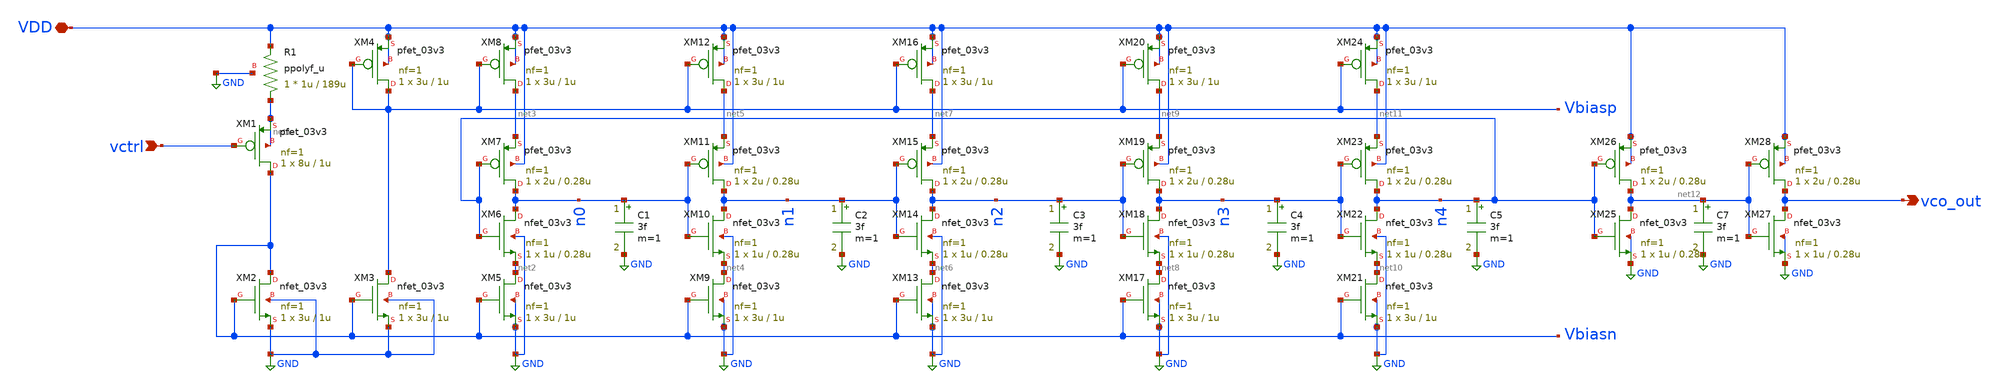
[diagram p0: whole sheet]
** sch_path: analog/vco/vco_core.sch
**.subckt vco_core VDD vctrl vco_out
*.iopin VDD
*.ipin vctrl
*.opin vco_out
XM1 Vbiasn vctrl net1 net1 pfet_03v3 L=1u W=8u nf=1 ad='int((nf+1)/2) * W/nf * 0.18u' as='int((nf+2)/2) * W/nf * 0.18u'
+ pd='2*int((nf+1)/2) * (W/nf + 0.18u)' ps='2*int((nf+2)/2) * (W/nf + 0.18u)' nrd='0.18u / W' nrs='0.18u / W'
+ sa=0 sb=0 sd=0 m=1
XM2 Vbiasn Vbiasn GND GND nfet_03v3 L=1u W=3u nf=1 ad='int((nf+1)/2) * W/nf * 0.18u' as='int((nf+2)/2) * W/nf * 0.18u'
+ pd='2*int((nf+1)/2) * (W/nf + 0.18u)' ps='2*int((nf+2)/2) * (W/nf + 0.18u)' nrd='0.18u / W' nrs='0.18u / W'
+ sa=0 sb=0 sd=0 m=1
XM3 Vbiasp Vbiasn GND GND nfet_03v3 L=1u W=3u nf=1 ad='int((nf+1)/2) * W/nf * 0.18u' as='int((nf+2)/2) * W/nf * 0.18u'
+ pd='2*int((nf+1)/2) * (W/nf + 0.18u)' ps='2*int((nf+2)/2) * (W/nf + 0.18u)' nrd='0.18u / W' nrs='0.18u / W'
+ sa=0 sb=0 sd=0 m=1
XM4 Vbiasp Vbiasp VDD VDD pfet_03v3 L=1u W=3u nf=1 ad='int((nf+1)/2) * W/nf * 0.18u' as='int((nf+2)/2) * W/nf * 0.18u'
+ pd='2*int((nf+1)/2) * (W/nf + 0.18u)' ps='2*int((nf+2)/2) * (W/nf + 0.18u)' nrd='0.18u / W' nrs='0.18u / W'
+ sa=0 sb=0 sd=0 m=1
XR1 net1 VDD GND ppolyf_u r_width=1u r_length=189u m=1
XM5 net2 Vbiasn GND GND nfet_03v3 L=1u W=3u nf=1 ad='int((nf+1)/2) * W/nf * 0.18u' as='int((nf+2)/2) * W/nf * 0.18u'
+ pd='2*int((nf+1)/2) * (W/nf + 0.18u)' ps='2*int((nf+2)/2) * (W/nf + 0.18u)' nrd='0.18u / W' nrs='0.18u / W'
+ sa=0 sb=0 sd=0 m=1
XM6 n0 n4 net2 GND nfet_03v3 L=0.28u W=1u nf=1 ad='int((nf+1)/2) * W/nf * 0.18u' as='int((nf+2)/2) * W/nf * 0.18u'
+ pd='2*int((nf+1)/2) * (W/nf + 0.18u)' ps='2*int((nf+2)/2) * (W/nf + 0.18u)' nrd='0.18u / W' nrs='0.18u / W'
+ sa=0 sb=0 sd=0 m=1
XM7 n0 n4 net3 VDD pfet_03v3 L=0.28u W=2u nf=1 ad='int((nf+1)/2) * W/nf * 0.18u' as='int((nf+2)/2) * W/nf * 0.18u'
+ pd='2*int((nf+1)/2) * (W/nf + 0.18u)' ps='2*int((nf+2)/2) * (W/nf + 0.18u)' nrd='0.18u / W' nrs='0.18u / W'
+ sa=0 sb=0 sd=0 m=1
XM8 net3 Vbiasp VDD VDD pfet_03v3 L=1u W=3u nf=1 ad='int((nf+1)/2) * W/nf * 0.18u' as='int((nf+2)/2) * W/nf * 0.18u'
+ pd='2*int((nf+1)/2) * (W/nf + 0.18u)' ps='2*int((nf+2)/2) * (W/nf + 0.18u)' nrd='0.18u / W' nrs='0.18u / W'
+ sa=0 sb=0 sd=0 m=1
XM9 net4 Vbiasn GND GND nfet_03v3 L=1u W=3u nf=1 ad='int((nf+1)/2) * W/nf * 0.18u' as='int((nf+2)/2) * W/nf * 0.18u'
+ pd='2*int((nf+1)/2) * (W/nf + 0.18u)' ps='2*int((nf+2)/2) * (W/nf + 0.18u)' nrd='0.18u / W' nrs='0.18u / W'
+ sa=0 sb=0 sd=0 m=1
XM10 n1 n0 net4 GND nfet_03v3 L=0.28u W=1u nf=1 ad='int((nf+1)/2) * W/nf * 0.18u' as='int((nf+2)/2) * W/nf * 0.18u'
+ pd='2*int((nf+1)/2) * (W/nf + 0.18u)' ps='2*int((nf+2)/2) * (W/nf + 0.18u)' nrd='0.18u / W' nrs='0.18u / W'
+ sa=0 sb=0 sd=0 m=1
XM11 n1 n0 net5 VDD pfet_03v3 L=0.28u W=2u nf=1 ad='int((nf+1)/2) * W/nf * 0.18u' as='int((nf+2)/2) * W/nf * 0.18u'
+ pd='2*int((nf+1)/2) * (W/nf + 0.18u)' ps='2*int((nf+2)/2) * (W/nf + 0.18u)' nrd='0.18u / W' nrs='0.18u / W'
+ sa=0 sb=0 sd=0 m=1
XM12 net5 Vbiasp VDD VDD pfet_03v3 L=1u W=3u nf=1 ad='int((nf+1)/2) * W/nf * 0.18u' as='int((nf+2)/2) * W/nf * 0.18u'
+ pd='2*int((nf+1)/2) * (W/nf + 0.18u)' ps='2*int((nf+2)/2) * (W/nf + 0.18u)' nrd='0.18u / W' nrs='0.18u / W'
+ sa=0 sb=0 sd=0 m=1
XM13 net6 Vbiasn GND GND nfet_03v3 L=1u W=3u nf=1 ad='int((nf+1)/2) * W/nf * 0.18u' as='int((nf+2)/2) * W/nf * 0.18u'
+ pd='2*int((nf+1)/2) * (W/nf + 0.18u)' ps='2*int((nf+2)/2) * (W/nf + 0.18u)' nrd='0.18u / W' nrs='0.18u / W'
+ sa=0 sb=0 sd=0 m=1
XM14 n2 n1 net6 GND nfet_03v3 L=0.28u W=1u nf=1 ad='int((nf+1)/2) * W/nf * 0.18u' as='int((nf+2)/2) * W/nf * 0.18u'
+ pd='2*int((nf+1)/2) * (W/nf + 0.18u)' ps='2*int((nf+2)/2) * (W/nf + 0.18u)' nrd='0.18u / W' nrs='0.18u / W'
+ sa=0 sb=0 sd=0 m=1
XM15 n2 n1 net7 VDD pfet_03v3 L=0.28u W=2u nf=1 ad='int((nf+1)/2) * W/nf * 0.18u' as='int((nf+2)/2) * W/nf * 0.18u'
+ pd='2*int((nf+1)/2) * (W/nf + 0.18u)' ps='2*int((nf+2)/2) * (W/nf + 0.18u)' nrd='0.18u / W' nrs='0.18u / W'
+ sa=0 sb=0 sd=0 m=1
XM16 net7 Vbiasp VDD VDD pfet_03v3 L=1u W=3u nf=1 ad='int((nf+1)/2) * W/nf * 0.18u' as='int((nf+2)/2) * W/nf * 0.18u'
+ pd='2*int((nf+1)/2) * (W/nf + 0.18u)' ps='2*int((nf+2)/2) * (W/nf + 0.18u)' nrd='0.18u / W' nrs='0.18u / W'
+ sa=0 sb=0 sd=0 m=1
XM17 net8 Vbiasn GND GND nfet_03v3 L=1u W=3u nf=1 ad='int((nf+1)/2) * W/nf * 0.18u' as='int((nf+2)/2) * W/nf * 0.18u'
+ pd='2*int((nf+1)/2) * (W/nf + 0.18u)' ps='2*int((nf+2)/2) * (W/nf + 0.18u)' nrd='0.18u / W' nrs='0.18u / W'
+ sa=0 sb=0 sd=0 m=1
XM18 n3 n2 net8 GND nfet_03v3 L=0.28u W=1u nf=1 ad='int((nf+1)/2) * W/nf * 0.18u' as='int((nf+2)/2) * W/nf * 0.18u'
+ pd='2*int((nf+1)/2) * (W/nf + 0.18u)' ps='2*int((nf+2)/2) * (W/nf + 0.18u)' nrd='0.18u / W' nrs='0.18u / W'
+ sa=0 sb=0 sd=0 m=1
XM19 n3 n2 net9 VDD pfet_03v3 L=0.28u W=2u nf=1 ad='int((nf+1)/2) * W/nf * 0.18u' as='int((nf+2)/2) * W/nf * 0.18u'
+ pd='2*int((nf+1)/2) * (W/nf + 0.18u)' ps='2*int((nf+2)/2) * (W/nf + 0.18u)' nrd='0.18u / W' nrs='0.18u / W'
+ sa=0 sb=0 sd=0 m=1
XM20 net9 Vbiasp VDD VDD pfet_03v3 L=1u W=3u nf=1 ad='int((nf+1)/2) * W/nf * 0.18u' as='int((nf+2)/2) * W/nf * 0.18u'
+ pd='2*int((nf+1)/2) * (W/nf + 0.18u)' ps='2*int((nf+2)/2) * (W/nf + 0.18u)' nrd='0.18u / W' nrs='0.18u / W'
+ sa=0 sb=0 sd=0 m=1
XM21 net10 Vbiasn GND GND nfet_03v3 L=1u W=3u nf=1 ad='int((nf+1)/2) * W/nf * 0.18u' as='int((nf+2)/2) * W/nf * 0.18u'
+ pd='2*int((nf+1)/2) * (W/nf + 0.18u)' ps='2*int((nf+2)/2) * (W/nf + 0.18u)' nrd='0.18u / W' nrs='0.18u / W'
+ sa=0 sb=0 sd=0 m=1
XM22 n4 n3 net10 GND nfet_03v3 L=0.28u W=1u nf=1 ad='int((nf+1)/2) * W/nf * 0.18u' as='int((nf+2)/2) * W/nf * 0.18u'
+ pd='2*int((nf+1)/2) * (W/nf + 0.18u)' ps='2*int((nf+2)/2) * (W/nf + 0.18u)' nrd='0.18u / W' nrs='0.18u / W'
+ sa=0 sb=0 sd=0 m=1
XM23 n4 n3 net11 VDD pfet_03v3 L=0.28u W=2u nf=1 ad='int((nf+1)/2) * W/nf * 0.18u' as='int((nf+2)/2) * W/nf * 0.18u'
+ pd='2*int((nf+1)/2) * (W/nf + 0.18u)' ps='2*int((nf+2)/2) * (W/nf + 0.18u)' nrd='0.18u / W' nrs='0.18u / W'
+ sa=0 sb=0 sd=0 m=1
XM24 net11 Vbiasp VDD VDD pfet_03v3 L=1u W=3u nf=1 ad='int((nf+1)/2) * W/nf * 0.18u' as='int((nf+2)/2) * W/nf * 0.18u'
+ pd='2*int((nf+1)/2) * (W/nf + 0.18u)' ps='2*int((nf+2)/2) * (W/nf + 0.18u)' nrd='0.18u / W' nrs='0.18u / W'
+ sa=0 sb=0 sd=0 m=1
C1 n0 GND 3f m=1
C2 n1 GND 3f m=1
C3 n2 GND 3f m=1
C4 n3 GND 3f m=1
C5 n4 GND 3f m=1
XM25 net12 n4 GND GND nfet_03v3 L=0.28u W=1u nf=1 ad='int((nf+1)/2) * W/nf * 0.18u' as='int((nf+2)/2) * W/nf * 0.18u'
+ pd='2*int((nf+1)/2) * (W/nf + 0.18u)' ps='2*int((nf+2)/2) * (W/nf + 0.18u)' nrd='0.18u / W' nrs='0.18u / W'
+ sa=0 sb=0 sd=0 m=1
XM26 net12 n4 VDD VDD pfet_03v3 L=0.28u W=2u nf=1 ad='int((nf+1)/2) * W/nf * 0.18u' as='int((nf+2)/2) * W/nf * 0.18u'
+ pd='2*int((nf+1)/2) * (W/nf + 0.18u)' ps='2*int((nf+2)/2) * (W/nf + 0.18u)' nrd='0.18u / W' nrs='0.18u / W'
+ sa=0 sb=0 sd=0 m=1
XM27 vco_out net12 GND GND nfet_03v3 L=0.28u W=1u nf=1 ad='int((nf+1)/2) * W/nf * 0.18u' as='int((nf+2)/2) * W/nf * 0.18u'
+ pd='2*int((nf+1)/2) * (W/nf + 0.18u)' ps='2*int((nf+2)/2) * (W/nf + 0.18u)' nrd='0.18u / W' nrs='0.18u / W'
+ sa=0 sb=0 sd=0 m=1
XM28 vco_out net12 VDD VDD pfet_03v3 L=0.28u W=2u nf=1 ad='int((nf+1)/2) * W/nf * 0.18u' as='int((nf+2)/2) * W/nf * 0.18u'
+ pd='2*int((nf+1)/2) * (W/nf + 0.18u)' ps='2*int((nf+2)/2) * (W/nf + 0.18u)' nrd='0.18u / W' nrs='0.18u / W'
+ sa=0 sb=0 sd=0 m=1
C7 net12 GND 3f m=1
**.ends
.GLOBAL GND
.end
